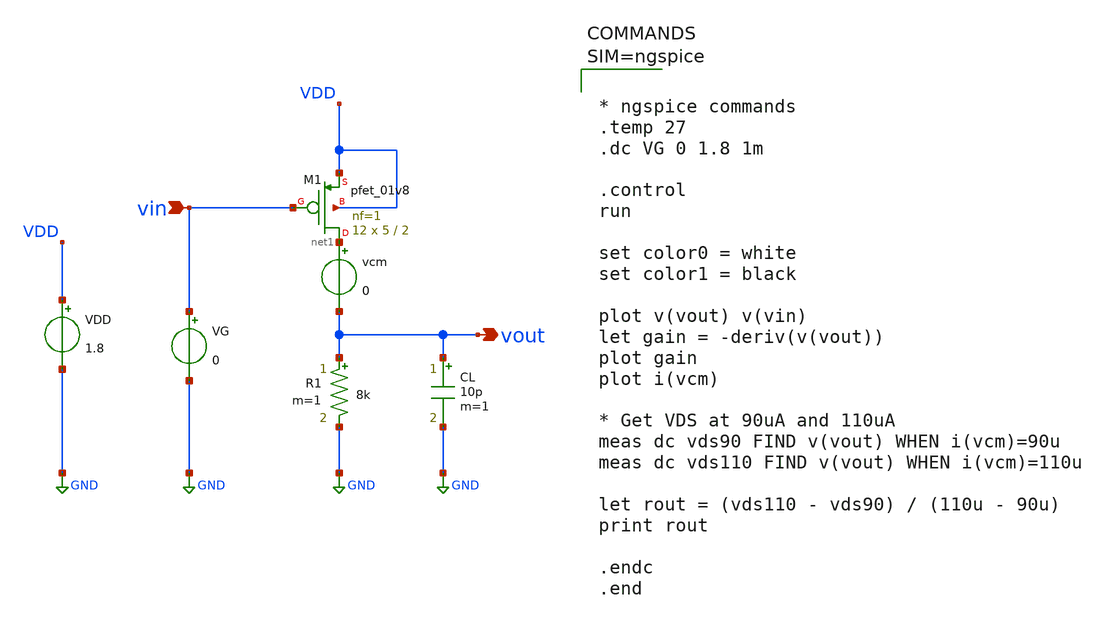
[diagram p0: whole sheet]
** sch_path: Common_Source_PMOS_Restitive_ckts/CS_Amp_PMOS_Restitive_Load_DC_Sweep.sch
**.subckt CS_Amp_PMOS_Restitive_Load_DC_Sweep vout vin
*.opin vout
*.ipin vin
R1 vout GND 8k m=1
CL vout GND 10p m=1
XM1 net1 vin VDD VDD sky130_fd_pr__pfet_01v8 L=2 W=5 nf=1 ad='int((1 + 1)/2) * 5 / 1 * 0.29' as='int((1 + 2)/2) * 5 / 1 * 0.29'
+ pd='2*int((1 + 1)/2) * (5 / 1 + 0.29)' ps='2*int((1 + 2)/2) * (5 / 1 + 0.29)' nrd='0.29 / 5 ' nrs='0.29 / 5 '
+ sa=0 sb=0 sd=0 mult=12 m=12
VG vin GND 0
VDD VDD GND 1.8
vcm net1 vout 0
**** begin user architecture code



* ngspice commands
.temp 27
.dc VG 0 1.8 1m

.control
run

set color0 = white
set color1 = black

plot v(vout) v(vin)
let gain = -deriv(v(vout))
plot gain
plot i(vcm)

* Get VDS at 90uA and 110uA
meas dc vds90 FIND v(vout) WHEN i(vcm)=90u
meas dc vds110 FIND v(vout) WHEN i(vcm)=110u

let rout = (vds110 - vds90) / (110u - 90u)
print rout

.endc
.end




** opencircuitdesign pdks install
.lib $::SKYWATER_MODELS/sky130.lib.spice tt

**** end user architecture code
**.ends
.GLOBAL GND
.end
